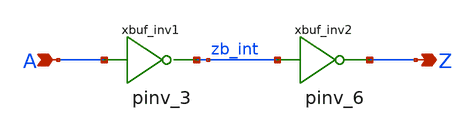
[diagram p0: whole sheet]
** sch_path: sram_2_64_scn4m_lcc/pbuf.sch
**.subckt pbuf A Z
*.ipin A
*.opin Z
xbuf_inv1 A zb_int vdd gnd pinv_3
xbuf_inv2 zb_int Z vdd gnd pinv_6
**.ends

* expanding   symbol:  pinv_3.sym # of pins=2
** sym_path: sram_2_64_scn4m_lcc/pinv_3.sym
** sch_path: sram_2_64_scn4m_lcc/pinv_3.sch
.subckt pinv_3 A Z vdd gnd
*.ipin A
*.opin Z
Mpinv_nmos Z A gnd gnd n w=1.6u l=0.4u m=1
Mp_inv_pmos Z A vdd vdd p w=3.2u l=0.4u m=1
.ends


* expanding   symbol:  pinv_6.sym # of pins=2
** sym_path: sram_2_64_scn4m/pinv_6.sym
** sch_path: sram_2_64_scn4m/pinv_6.sch
.subckt pinv_6 A Z vdd gnd
*.ipin A
*.opin Z
Mpinv_nmos Z A gnd gnd n w=3.2u l=0.4u m=1
Mp_inv_pmos Z A vdd vdd p w=6.4u l=0.4u m=1
.ends

.end
